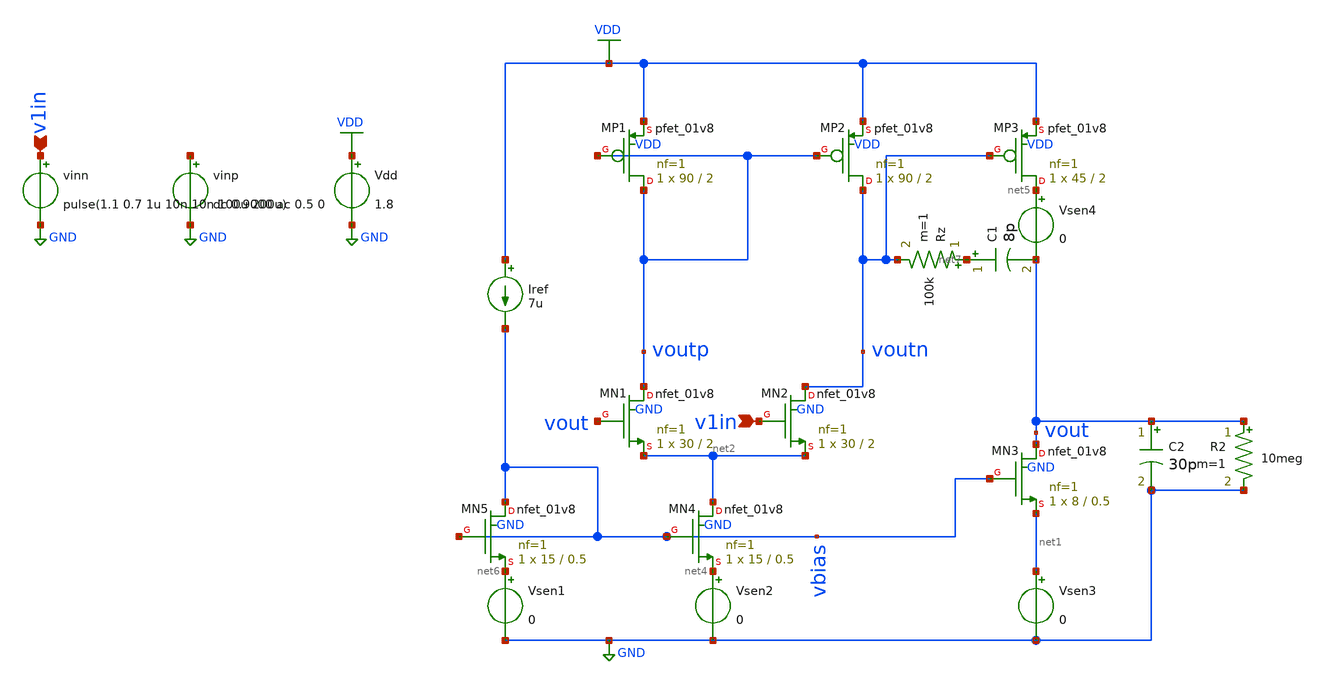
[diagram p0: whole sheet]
** sch_path: testbenches/prelayout/diffpairUnitygain.sch
**.subckt diffpairUnitygain v1in v1in
*.ipin v1in
*.ipin v1in
Vdd VDD GND 1.8
vinp net3 GND dc 0.9000 ac 0.5 0
vinn v1in GND pulse(1.1 0.7 1u 10n 10n 100u 200u)
XMN1 voutp vout net2 GND sky130_fd_pr__nfet_01v8 L=2 W=30 nf=1 ad='int((nf+1)/2) * W/nf * 0.29' as='int((nf+2)/2) * W/nf * 0.29'
+ pd='2*int((nf+1)/2) * (W/nf + 0.29)' ps='2*int((nf+2)/2) * (W/nf + 0.29)' nrd='0.29 / W' nrs='0.29 / W'
+ sa=0 sb=0 sd=0 mult=1 m=1
XMN2 voutn v1in net2 GND sky130_fd_pr__nfet_01v8 L=2 W=30 nf=1 ad='int((nf+1)/2) * W/nf * 0.29' as='int((nf+2)/2) * W/nf * 0.29'
+ pd='2*int((nf+1)/2) * (W/nf + 0.29)' ps='2*int((nf+2)/2) * (W/nf + 0.29)' nrd='0.29 / W' nrs='0.29 / W'
+ sa=0 sb=0 sd=0 mult=1 m=1
XMP1 voutp voutp VDD VDD sky130_fd_pr__pfet_01v8 L=2 W=90 nf=1 ad='int((nf+1)/2) * W/nf * 0.29' as='int((nf+2)/2) * W/nf * 0.29'
+ pd='2*int((nf+1)/2) * (W/nf + 0.29)' ps='2*int((nf+2)/2) * (W/nf + 0.29)' nrd='0.29 / W' nrs='0.29 / W'
+ sa=0 sb=0 sd=0 mult=1 m=1
XMP2 voutn voutp VDD VDD sky130_fd_pr__pfet_01v8 L=2 W=90 nf=1 ad='int((nf+1)/2) * W/nf * 0.29' as='int((nf+2)/2) * W/nf * 0.29'
+ pd='2*int((nf+1)/2) * (W/nf + 0.29)' ps='2*int((nf+2)/2) * (W/nf + 0.29)' nrd='0.29 / W' nrs='0.29 / W'
+ sa=0 sb=0 sd=0 mult=1 m=1
Iref VDD vbias 7u
Vsen2 net4 GND 0
XMP3 net5 voutn VDD VDD sky130_fd_pr__pfet_01v8 L=2 W=45 nf=1 ad='int((nf+1)/2) * W/nf * 0.29' as='int((nf+2)/2) * W/nf * 0.29'
+ pd='2*int((nf+1)/2) * (W/nf + 0.29)' ps='2*int((nf+2)/2) * (W/nf + 0.29)' nrd='0.29 / W' nrs='0.29 / W'
+ sa=0 sb=0 sd=0 mult=1 m=1
XMN3 vout vbias net1 GND sky130_fd_pr__nfet_01v8 L=0.5 W=8 nf=1 ad='int((nf+1)/2) * W/nf * 0.29' as='int((nf+2)/2) * W/nf * 0.29'
+ pd='2*int((nf+1)/2) * (W/nf + 0.29)' ps='2*int((nf+2)/2) * (W/nf + 0.29)' nrd='0.29 / W' nrs='0.29 / W'
+ sa=0 sb=0 sd=0 mult=1 m=1
Vsen3 net1 GND 0
Vsen1 net6 GND 0
C1 net7 vout 8p m=1
XMN4 net2 vbias net4 GND sky130_fd_pr__nfet_01v8 L=0.5 W=15 nf=1 ad='int((nf+1)/2) * W/nf * 0.29' as='int((nf+2)/2) * W/nf * 0.29'
+ pd='2*int((nf+1)/2) * (W/nf + 0.29)' ps='2*int((nf+2)/2) * (W/nf + 0.29)' nrd='0.29 / W' nrs='0.29 / W'
+ sa=0 sb=0 sd=0 mult=1 m=1
XMN5 vbias vbias net6 GND sky130_fd_pr__nfet_01v8 L=0.5 W=15 nf=1 ad='int((nf+1)/2) * W/nf * 0.29' as='int((nf+2)/2) * W/nf * 0.29'
+ pd='2*int((nf+1)/2) * (W/nf + 0.29)' ps='2*int((nf+2)/2) * (W/nf + 0.29)' nrd='0.29 / W' nrs='0.29 / W'
+ sa=0 sb=0 sd=0 mult=1 m=1
C2 vout GND 30p m=1
Rz net7 voutn 100k m=1
Vsen4 net5 vout 0
R2 vout GND 10meg m=1
**** begin user architecture code


.lib /home/ttuser/pdk/sky130A/libs.tech/ngspice/sky130.lib.spice tt
.control
save all

op
tran 1n 15u

plot v(v1in) v(vout)

* Large falling step: 1.1 V -> 0.7 V
* Step size = 0.4 V

meas tran vfinal find v(vout) at=15u
meas tran vmin min v(vout) from=1u to=15u
meas tran vmax max v(vout) from=1u to=15u

* Step midpoint
meas tran tstep when v(v1in)=0.9 fall=1

* Fall time: 90% to 10%
* 90% level = 1.06 V
* 10% level = 0.74 V
meas tran t90 when v(vout)=1.06 fall=1
meas tran t10 when v(vout)=0.74 fall=1

* 2% settling band around final value 0.7 V
* 2% of 0.4 V = 8 mV
* Band = 0.692 V to 0.708 V
meas tran t_upper when v(vout)=0.708 fall=last
meas tran t_lower when v(vout)=0.692 rise=last

* Slew rate
let dvout = deriv(v(vout))
let neg_dvout = -dvout
meas tran sr_fall max neg_dvout from=1u to=5u

* Calculated values
let fall_time = t10 - t90
let undershoot_pct = (vfinal - vmin)/0.4*100
let overshoot_before_fall_pct = (vmax - 1.1)/0.4*100

let ts_upper = t_upper - tstep
let ts_lower = t_lower - tstep

print fall_time
print undershoot_pct
print overshoot_before_fall_pct
print ts_upper
print ts_lower
print sr_fall

.endc


**** end user architecture code
**.ends
.GLOBAL VDD
.GLOBAL GND
.end
